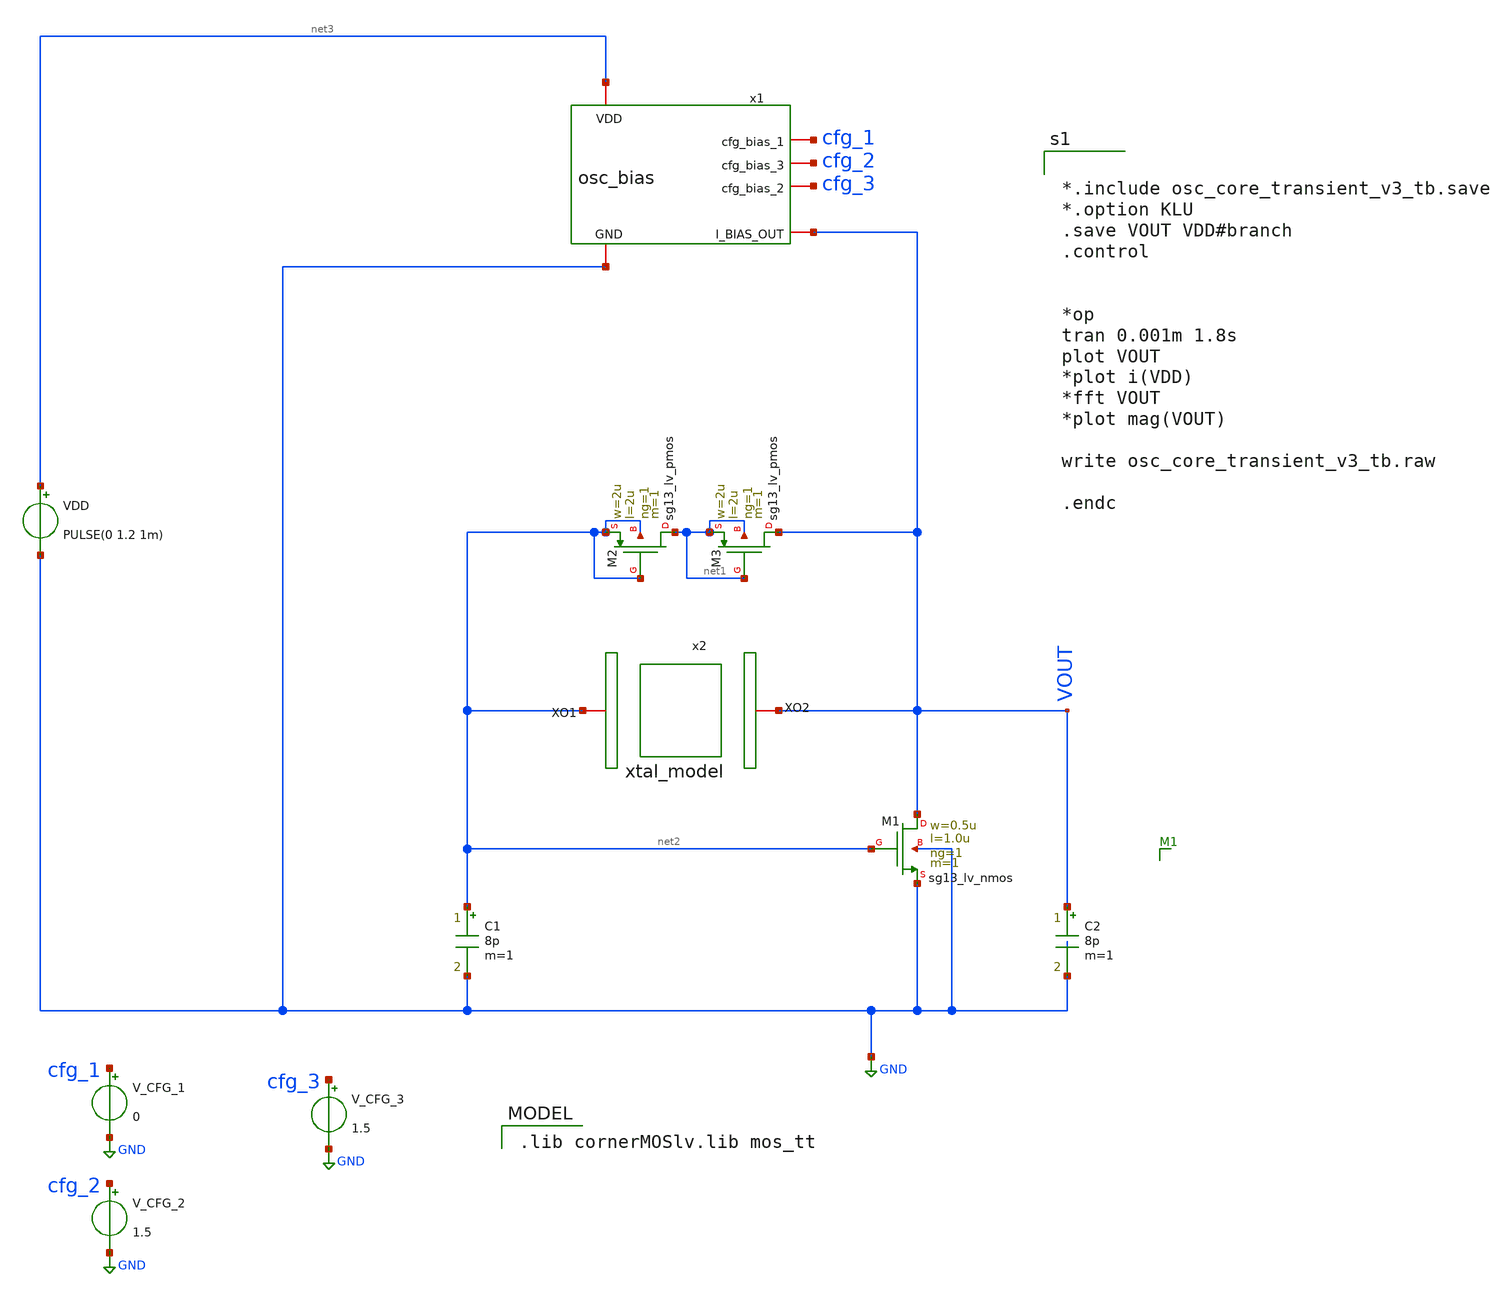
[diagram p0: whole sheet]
** sch_path: osc_core_transient_v3_tb.sch
**.subckt osc_core_transient_v3_tb
XM1 VOUT net2 GND GND sg13_lv_nmos w=0.5u l=1.0u ng=1 m=1 mm_ok=1
C1 net2 GND 8p m=1
C2 VOUT GND 8p m=1
VDD net3 GND PULSE(0 1.2 1m)
XM2 net1 net2 net2 net2 sg13_lv_pmos w=2u l=2u ng=1 m=1 mm_ok=1
XM3 VOUT net1 net1 net1 sg13_lv_pmos w=2u l=2u ng=1 m=1 mm_ok=1
x1 net3 cfg_1 cfg_2 cfg_3 GND VOUT osc_bias
x2 net2 VOUT xtal_model
V_CFG_1 cfg_1 GND 0
V_CFG_2 cfg_2 GND 1.5
V_CFG_3 cfg_3 GND 1.5
**** begin user architecture code


*.include osc_core_transient_v3_tb.save
*.option KLU
.save VOUT VDD#branch
.control


*op
tran 0.001m 1.8s
plot VOUT
*plot i(VDD)
*fft VOUT
*plot mag(VOUT)

write osc_core_transient_v3_tb.raw

.endc


 .lib cornerMOSlv.lib mos_tt

**** end user architecture code
**.ends

* expanding   symbol:  osc_bias.sym # of pins=6
** sym_path: osc_bias.sym
** sch_path: osc_bias.sch
.subckt osc_bias VDD cfg_bias_1 cfg_bias_3 cfg_bias_2 GND I_BIAS_OUT
*.iopin VDD
*.iopin GND
*.iopin I_BIAS_OUT
*.iopin cfg_bias_1
*.iopin cfg_bias_2
*.iopin cfg_bias_3
XM1 vp_bias vp_bias VDD VDD sg13_lv_pmos w=1u l=10u ng=1 m=1 mm_ok=1
XM3 vp_bias vp_bias net2 net1 sg13_lv_nmos w=0.25u l=10u ng=1 m=1 mm_ok=1
XM4 net2 net2 net3 net1 sg13_lv_nmos w=0.25u l=10u ng=1 m=1 mm_ok=1
XM5 net3 net3 net1 net1 sg13_lv_nmos w=0.25u l=10u ng=1 m=1 mm_ok=1
XM2 net7 vp_bias VDD VDD sg13_lv_pmos w=0.5u l=10u ng=1 m=1 mm_ok=1
XM6 I_BIAS_OUT cfg_bias_1 net7 VDD sg13_lv_pmos w=0.5u l=5u ng=1 m=1 mm_ok=1
XM7 net4 vp_bias VDD VDD sg13_lv_pmos w=0.5u l=10u ng=1 m=1 mm_ok=1
XM8 net5 vp_bias VDD VDD sg13_lv_pmos w=0.5u l=10u ng=1 m=1 mm_ok=1
XM9 I_BIAS_OUT cfg_bias_2 net4 VDD sg13_lv_pmos w=0.5u l=10u ng=1 m=1 mm_ok=1
XM10 I_BIAS_OUT cfg_bias_3 net5 VDD sg13_lv_pmos w=0.5u l=10u ng=1 m=1 mm_ok=1
XM11 net1 net1 net6 net1 sg13_lv_nmos w=0.25u l=10u ng=1 m=1 mm_ok=1
Vmeas net6 GND 0
.save i(vmeas)
.ends


* expanding   symbol:  xtal_model.sym # of pins=2
** sym_path: xtal_model.sym
** sch_path: xtal_model.sch
.subckt xtal_model XO1 XO2
*.iopin XO2
*.iopin XO1
R1 XO1 net1 1k m=1
Cm net1 net2 1p m=1
C0 XO1 XO2 1p m=1
Lm net2 XO2 1n m=1
.ends

.GLOBAL GND
.end
